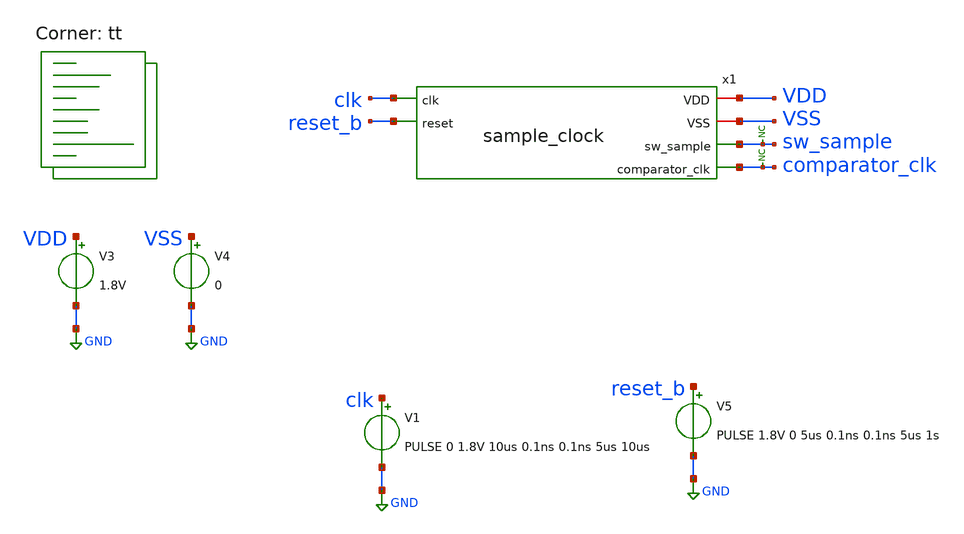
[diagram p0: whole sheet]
** sch_path: xschem/tests/sample_clock/sample_clock_test.sch
**.subckt sample_clock_test
V3 VDD GND 1.8V
V4 VSS GND 0
x1 VDD clk reset_b VSS sw_sample comparator_clk sample_clock
V1 clk GND PULSE 0 1.8V 10us 0.1ns 0.1ns 5us 10us
V5 reset_b GND PULSE 1.8V 0 5us 0.1ns 0.1ns 5us 1s
* noconn sw_sample
* noconn comparator_clk
**** begin user architecture code
 *.lib $::SKYWATER_MODELS/sky130.lib.spice tt
.include $::SKYWATER_STDCELLS/sky130_fd_sc_hd.spice


.options acct list
.temp 25
.control
save all
tran 0.1u 400u
plot reset_b-2 clk sw_sample+2 comparator_clk+4
write sample_clock_test.raw
.endc


.lib $::SKYWATER_MODELS/sky130.lib.spice tt
**** end user architecture code
**.ends

* expanding   symbol:  src/sample_clock/sample_clock.sym # of pins=6
** sym_path: xschem/src/sample_clock/sample_clock.sym
** sch_path: xschem/src/sample_clock/sample_clock.sch
.subckt sample_clock VDD clk reset VSS sw_sample comparator_clk
*.iopin VDD
*.ipin clk
*.opin sw_sample
*.iopin VSS
*.opin comparator_clk
*.ipin reset
x5 clk johnson_counter_loop reset VSS VSS VDD VDD sw_sample sky130_fd_sc_hd__dfrtp_1
x7 clk sw_sample reset VSS VSS VDD VDD net1 sky130_fd_sc_hd__dfrtp_1
x8 clk net1 reset VSS VSS VDD VDD net2 sky130_fd_sc_hd__dfrtp_1
x9 clk net2 reset VSS VSS VDD VDD net3 sky130_fd_sc_hd__dfrtp_1
x10 clk net3 reset VSS VSS VDD VDD net4 sky130_fd_sc_hd__dfrtp_1
x11 clk net4 reset VSS VSS VDD VDD net5 sky130_fd_sc_hd__dfrtp_1
x12 clk net5 reset VSS VSS VDD VDD net6 sky130_fd_sc_hd__dfrtp_1
x13 clk net6 reset VSS VSS VDD VDD net7 sky130_fd_sc_hd__dfrtp_1
x14 clk net7 reset VSS VSS VDD VDD net8 sky130_fd_sc_hd__dfrtp_1
x15 clk net8 reset VSS VSS VDD VDD net9 sky130_fd_sc_hd__dfrtp_1
x16 clk net9 reset VSS VSS VDD VDD net10 sky130_fd_sc_hd__dfrtp_1
x17 clk net10 reset VSS VSS VDD VDD net11 sky130_fd_sc_hd__dfrtp_1
x18 clk net11 reset VSS VSS VDD VDD net12 sky130_fd_sc_hd__dfrtp_1
x19 clk net12 reset VSS VSS VDD VDD net13 sky130_fd_sc_hd__dfrtp_1
x20 clk net13 reset VSS VSS VDD VDD net14 sky130_fd_sc_hd__dfrtp_1
x21 clk net14 reset VSS VSS VDD VDD net15 sky130_fd_sc_hd__dfrtp_1
x22 net15 VSS VSS VDD VDD johnson_counter_loop sky130_fd_sc_hd__inv_1
x23 clk net16 VSS VSS VDD VDD net19 sky130_fd_sc_hd__and2_1
x24 sw_sample VSS VSS VDD VDD net16 sky130_fd_sc_hd__inv_1
x25 net18 VSS VSS VDD VDD comparator_clk sky130_fd_sc_hd__buf_16
x26 net20 VSS VSS VDD VDD net17 sky130_fd_sc_hd__buf_4
x27 net17 VSS VSS VDD VDD net18 sky130_fd_sc_hd__buf_8
x1 net19 VSS VSS VDD VDD net20 sky130_fd_sc_hd__buf_2
.ends

.GLOBAL GND
.end
